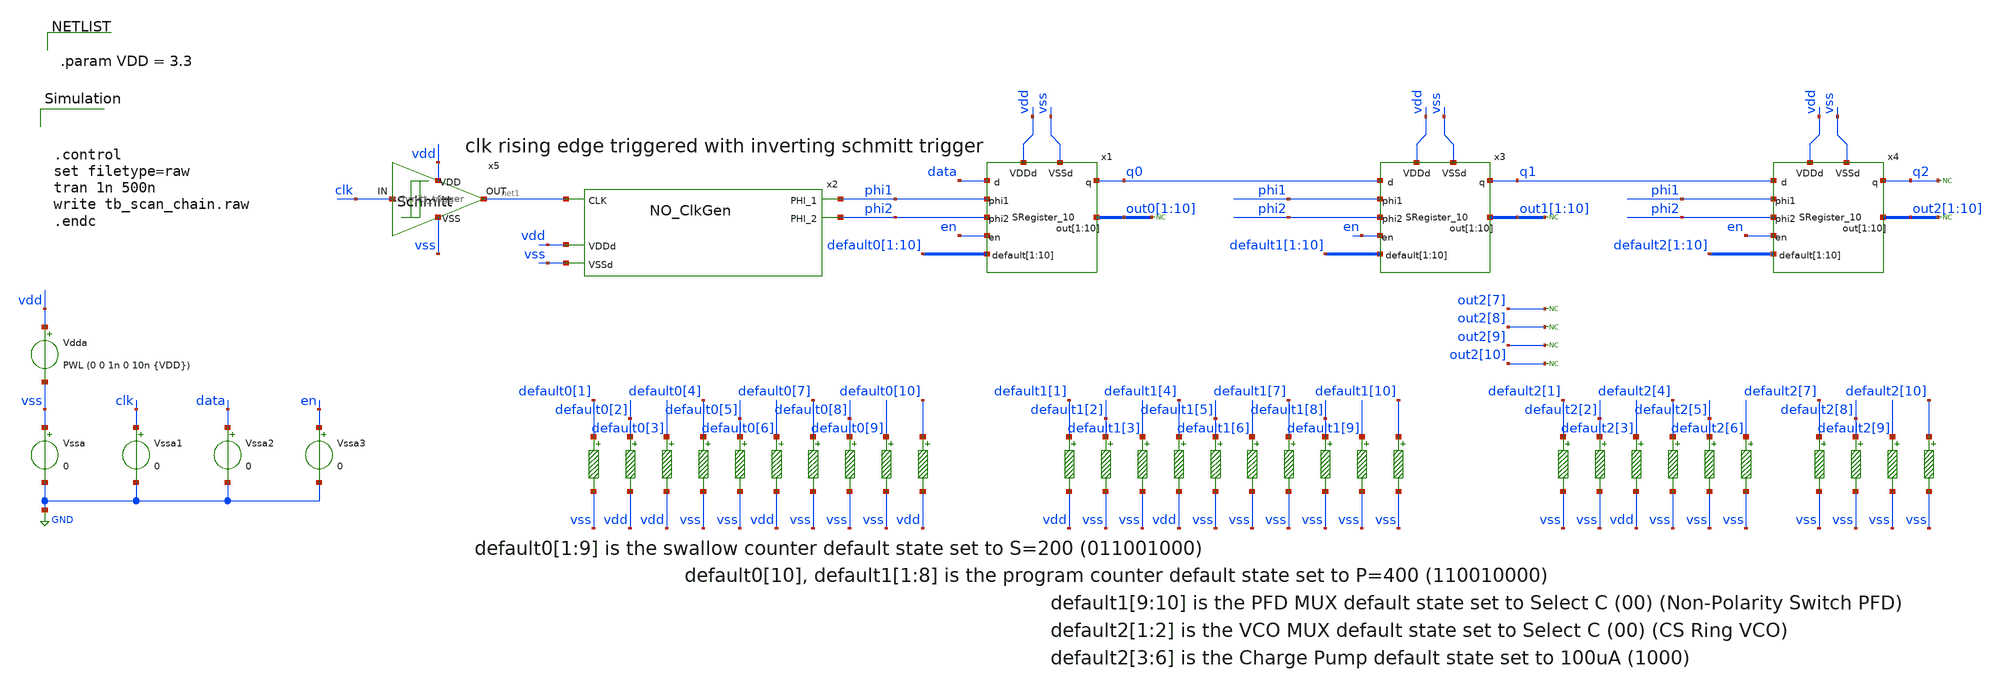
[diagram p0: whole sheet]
** sch_path: designs/libs/tb_top_level/tb_scan_chain.sch
**.subckt tb_scan_chain
x2 phi2 net1 phi1 vdd vss NO_ClkGen
x1 vdd vss phi1 phi2 en default0[1] default0[2] default0[3] default0[4] default0[5] default0[6]
+ default0[7] default0[8] default0[9] default0[10] data q0 out0[1] out0[2] out0[3] out0[4] out0[5] out0[6]
+ out0[7] out0[8] out0[9] out0[10] SRegister_10
x3 vdd vss phi1 phi2 en default1[1] default1[2] default1[3] default1[4] default1[5] default1[6]
+ default1[7] default1[8] default1[9] default1[10] q0 q1 out1[1] out1[2] out1[3] out1[4] out1[5] out1[6] out1[7]
+ out1[8] out1[9] out1[10] SRegister_10
x4 vdd vss phi1 phi2 en default2[1] default2[2] default2[3] default2[4] default2[5] default2[6]
+ default2[7] default2[8] default2[9] default2[10] q1 q2 out2[1] out2[2] out2[3] out2[4] out2[5] out2[6] out2[7]
+ out2[8] out2[9] out2[10] SRegister_10
* noconn q2
x5 clk net1 vdd vss schmitt_trigger
* noconn out2[7]
* noconn out2[8]
* noconn out2[9]
* noconn out2[10]
R1 default1[1] vdd 0.01 m=1
R2 default1[2] vss 0.01 m=1
R3 default1[3] vss 0.01 m=1
R4 default1[4] vdd 0.01 m=1
R5 default1[5] vss 0.01 m=1
R6 default1[6] vss 0.01 m=1
R7 default1[7] vss 0.01 m=1
R8 default1[8] vss 0.01 m=1
R9 default1[9] vss 0.01 m=1
R10 default1[10] vss 0.01 m=1
R11 default2[1] vss 0.01 m=1
R12 default2[2] vss 0.01 m=1
R13 default2[3] vdd 0.01 m=1
R14 default2[4] vss 0.01 m=1
R15 default2[5] vss 0.01 m=1
R16 default2[6] vss 0.01 m=1
R17 default2[7] vss 0.01 m=1
R18 default2[8] vss 0.01 m=1
R19 default2[9] vss 0.01 m=1
R20 default2[10] vss 0.01 m=1
R21 default0[1] vss 0.01 m=1
R22 default0[2] vdd 0.01 m=1
R23 default0[3] vdd 0.01 m=1
R24 default0[4] vss 0.01 m=1
R25 default0[5] vss 0.01 m=1
R26 default0[6] vdd 0.01 m=1
R27 default0[7] vss 0.01 m=1
R28 default0[8] vss 0.01 m=1
R29 default0[9] vss 0.01 m=1
R30 default0[10] vdd 0.01 m=1
Vssa vss GND 0
Vdda vdd vss PWL (0 0 1n 0 10n {VDD})
Vssa1 clk GND 0
Vssa2 data GND 0
Vssa3 en GND 0
* noconn out0[1:10]
* noconn out1[1:10]
* noconn out2[1:10]
**** begin user architecture code

.include /foss/pdks/gf180mcuD/libs.ref/gf180mcu_fd_sc_mcu9t5v0/spice/gf180mcu_fd_sc_mcu9t5v0.spice
.include $::180MCU_MODELS/design.ngspice
.lib $::180MCU_MODELS/sm141064.ngspice typical
.lib $::180MCU_MODELS/sm141064.ngspice cap_mim
.lib $::180MCU_MODELS/sm141064.ngspice mimcap_typical



.param VDD = 3.3





.control
set filetype=raw
tran 1n 500n
write tb_scan_chain.raw
.endc


**** end user architecture code
**.ends
.GLOBAL GND
.end
